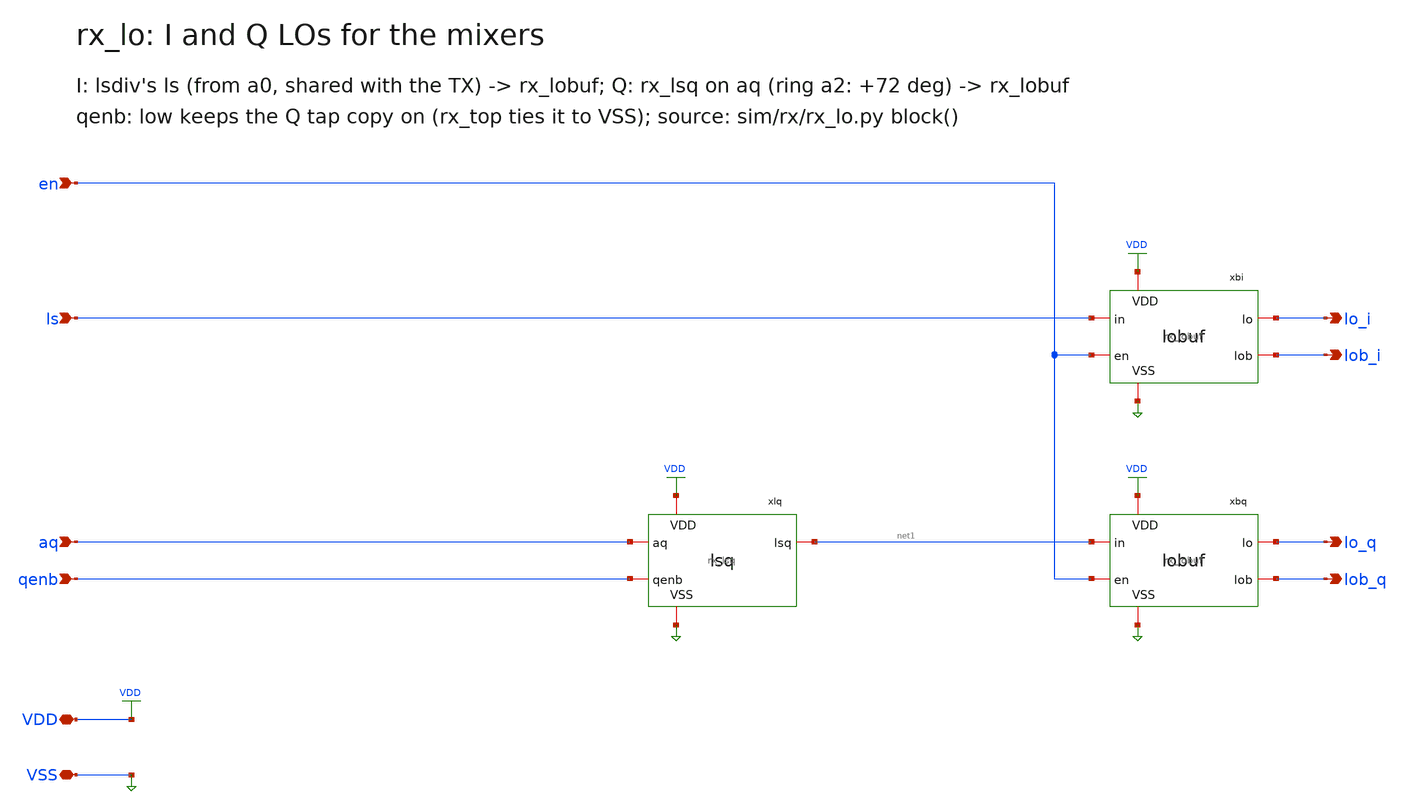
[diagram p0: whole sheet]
** sch_path: xschem/rx_lo.sch
**.subckt rx_lo VDD VSS ls aq en qenb lo_i lob_i lo_q lob_q
*.iopin VDD
*.iopin VSS
*.ipin ls
*.ipin aq
*.ipin en
*.ipin qenb
*.opin lo_i
*.opin lob_i
*.opin lo_q
*.opin lob_q
xlq VDD VSS aq qenb net1 rx_lsq
xbi VDD VSS ls en lo_i lob_i rx_lobuf
xbq VDD VSS net1 en lo_q lob_q rx_lobuf
**.ends

* expanding   symbol:  rx_lsq.sym # of pins=5
** sym_path: xschem/rx_lsq.sym
** sch_path: xschem/rx_lsq.sch
.subckt rx_lsq VDD VSS aq qenb lsq
*.iopin VDD
*.iopin VSS
*.ipin aq
*.ipin qenb
*.opin lsq
XHq net2 qenb VDD VDD pfet_03v3 L=0.28u W=10.0u nf=1 ad=5.0p as=5.0p pd=21.0u ps=21.0u nrd=0 nrs=0
+ sa=0 sb=0 sd=0 m=2
XCq VSS net2 VSS VSS nfet_03v3 L=10.0u W=24.57u nf=1 ad=12.285p as=12.285p pd=50.14u ps=50.14u nrd=0
+ nrs=0 sa=0 sb=0 sd=0 m=1
xls net2 VSS aq lsq ls_ac
xd1 net2 VSS lsq net3 tspc_t1
XTTp net1 lsq net2 net2 pfet_03v3 L=0.28u W=1.0499999999999998u nf=1 ad=0.5249999999999999p
+ as=0.5249999999999999p pd=3.0999999999999996u ps=3.0999999999999996u nrd=0 nrs=0 sa=0 sb=0 sd=0 m=1
XTTn net1 lsq VSS VSS nfet_03v3 L=0.28u W=0.41999999999999993u nf=1 ad=0.20999999999999996p
+ as=0.20999999999999996p pd=1.8399999999999999u ps=1.8399999999999999u nrd=0 nrs=0 sa=0 sb=0 sd=0 m=1
XDq lsq qenb VSS VSS nfet_03v3 L=0.28u W=0.41999999999999993u nf=1 ad=0.20999999999999996p
+ as=0.20999999999999996p pd=1.8399999999999999u ps=1.8399999999999999u nrd=0 nrs=0 sa=0 sb=0 sd=0 m=1
.ends


* expanding   symbol:  rx_lobuf.sym # of pins=6
** sym_path: xschem/rx_lobuf.sym
** sch_path: xschem/rx_lobuf.sch
.subckt rx_lobuf VDD VSS in en lo lob
*.iopin VDD
*.iopin VSS
*.ipin in
*.ipin en
*.opin lo
*.opin lob
XG0a net1 in VDD VDD pfet_03v3 L=0.28u W=0.6u nf=1 ad=0.3p as=0.3p pd=2.2u ps=2.2u nrd=0 nrs=0 sa=0
+ sb=0 sd=0 m=1
XG0b net1 en VDD VDD pfet_03v3 L=0.28u W=0.6u nf=1 ad=0.3p as=0.3p pd=2.2u ps=2.2u nrd=0 nrs=0 sa=0
+ sb=0 sd=0 m=1
XG0c net1 in net2 VSS nfet_03v3 L=0.28u W=0.5u nf=1 ad=0.25p as=0.25p pd=2.0u ps=2.0u nrd=0 nrs=0
+ sa=0 sb=0 sd=0 m=1
XG0d net2 en VSS VSS nfet_03v3 L=0.28u W=0.5u nf=1 ad=0.25p as=0.25p pd=2.0u ps=2.0u nrd=0 nrs=0
+ sa=0 sb=0 sd=0 m=1
XTp net3 net1 VDD VDD pfet_03v3 L=0.28u W=1.0499999999999998u nf=1 ad=0.5249999999999999p
+ as=0.5249999999999999p pd=3.0999999999999996u ps=3.0999999999999996u nrd=0 nrs=0 sa=0 sb=0 sd=0 m=1
XTn net3 net1 VSS VSS nfet_03v3 L=0.28u W=0.41999999999999993u nf=1 ad=0.20999999999999996p
+ as=0.20999999999999996p pd=1.8399999999999999u ps=1.8399999999999999u nrd=0 nrs=0 sa=0 sb=0 sd=0 m=1
XA1p net4 net3 VDD VDD pfet_03v3 L=0.28u W=1.25u nf=1 ad=0.625p as=0.625p pd=3.5u ps=3.5u nrd=0
+ nrs=0 sa=0 sb=0 sd=0 m=1
XA1n net4 net3 VSS VSS nfet_03v3 L=0.28u W=0.5u nf=1 ad=0.25p as=0.25p pd=2.0u ps=2.0u nrd=0 nrs=0
+ sa=0 sb=0 sd=0 m=1
XA2p net5 net4 VDD VDD pfet_03v3 L=0.28u W=2.5u nf=1 ad=1.25p as=1.25p pd=6.0u ps=6.0u nrd=0 nrs=0
+ sa=0 sb=0 sd=0 m=1
XA2n net5 net4 VSS VSS nfet_03v3 L=0.28u W=1.0u nf=1 ad=0.5p as=0.5p pd=3.0u ps=3.0u nrd=0 nrs=0
+ sa=0 sb=0 sd=0 m=1
XB1p net6 net3 VDD VDD pfet_03v3 L=0.28u W=3.7499999999999996u nf=1 ad=1.8749999999999998p
+ as=1.8749999999999998p pd=8.5u ps=8.5u nrd=0 nrs=0 sa=0 sb=0 sd=0 m=1
XB1n net6 net3 VSS VSS nfet_03v3 L=0.28u W=1.5u nf=1 ad=0.75p as=0.75p pd=4.0u ps=4.0u nrd=0 nrs=0
+ sa=0 sb=0 sd=0 m=1
XTGp net7 VSS net6 VDD pfet_03v3 L=0.28u W=2.5u nf=1 ad=1.25p as=1.25p pd=6.0u ps=6.0u nrd=0 nrs=0
+ sa=0 sb=0 sd=0 m=1
XTGn net7 VDD net6 VSS nfet_03v3 L=0.28u W=1.0u nf=1 ad=0.5p as=0.5p pd=3.0u ps=3.0u nrd=0 nrs=0
+ sa=0 sb=0 sd=0 m=1
XXBp net7 net5 VDD VDD pfet_03v3 L=0.28u W=1.0499999999999998u nf=1 ad=0.5249999999999999p
+ as=0.5249999999999999p pd=3.0999999999999996u ps=3.0999999999999996u nrd=0 nrs=0 sa=0 sb=0 sd=0 m=1
XXBn net7 net5 VSS VSS nfet_03v3 L=0.28u W=0.41999999999999993u nf=1 ad=0.20999999999999996p
+ as=0.20999999999999996p pd=1.8399999999999999u ps=1.8399999999999999u nrd=0 nrs=0 sa=0 sb=0 sd=0 m=1
XXAp net5 net7 VDD VDD pfet_03v3 L=0.28u W=1.0499999999999998u nf=1 ad=0.5249999999999999p
+ as=0.5249999999999999p pd=3.0999999999999996u ps=3.0999999999999996u nrd=0 nrs=0 sa=0 sb=0 sd=0 m=1
XXAn net5 net7 VSS VSS nfet_03v3 L=0.28u W=0.41999999999999993u nf=1 ad=0.20999999999999996p
+ as=0.20999999999999996p pd=1.8399999999999999u ps=1.8399999999999999u nrd=0 nrs=0 sa=0 sb=0 sd=0 m=1
XPGa net8 net5 VDD VDD pfet_03v3 L=0.28u W=1.25u nf=1 ad=0.625p as=0.625p pd=3.5u ps=3.5u nrd=0
+ nrs=0 sa=0 sb=0 sd=0 m=1
XPGb net8 en VDD VDD pfet_03v3 L=0.28u W=1.25u nf=1 ad=0.625p as=0.625p pd=3.5u ps=3.5u nrd=0 nrs=0
+ sa=0 sb=0 sd=0 m=1
XPGc net8 net5 net9 VSS nfet_03v3 L=0.28u W=1.0u nf=1 ad=0.5p as=0.5p pd=3.0u ps=3.0u nrd=0 nrs=0
+ sa=0 sb=0 sd=0 m=1
XPGd net9 en VSS VSS nfet_03v3 L=0.28u W=1.0u nf=1 ad=0.5p as=0.5p pd=3.0u ps=3.0u nrd=0 nrs=0 sa=0
+ sb=0 sd=0 m=1
XP1p net10 net8 VDD VDD pfet_03v3 L=0.28u W=2.0u nf=1 ad=1.0p as=1.0p pd=5.0u ps=5.0u nrd=0 nrs=0
+ sa=0 sb=0 sd=0 m=1
XP1n net10 net8 VSS VSS nfet_03v3 L=0.28u W=0.7999999999999999u nf=1 ad=0.39999999999999997p
+ as=0.39999999999999997p pd=2.5999999999999996u ps=2.5999999999999996u nrd=0 nrs=0 sa=0 sb=0 sd=0 m=1
XP2p net11 net10 VDD VDD pfet_03v3 L=0.28u W=5.0u nf=1 ad=2.5p as=2.5p pd=11.0u ps=11.0u nrd=0 nrs=0
+ sa=0 sb=0 sd=0 m=1
XP2n net11 net10 VSS VSS nfet_03v3 L=0.28u W=2.0u nf=1 ad=1.0p as=1.0p pd=5.0u ps=5.0u nrd=0 nrs=0
+ sa=0 sb=0 sd=0 m=1
XP3p lo net11 VDD VDD pfet_03v3 L=0.28u W=12.499999999999998u nf=1 ad=6.249999999999999p
+ as=6.249999999999999p pd=25.999999999999996u ps=25.999999999999996u nrd=0 nrs=0 sa=0 sb=0 sd=0 m=1
XP3n lo net11 VSS VSS nfet_03v3 L=0.28u W=5.0u nf=1 ad=2.5p as=2.5p pd=11.0u ps=11.0u nrd=0 nrs=0
+ sa=0 sb=0 sd=0 m=1
XNGa net12 net7 VDD VDD pfet_03v3 L=0.28u W=1.25u nf=1 ad=0.625p as=0.625p pd=3.5u ps=3.5u nrd=0
+ nrs=0 sa=0 sb=0 sd=0 m=1
XNGb net12 en VDD VDD pfet_03v3 L=0.28u W=1.25u nf=1 ad=0.625p as=0.625p pd=3.5u ps=3.5u nrd=0 nrs=0
+ sa=0 sb=0 sd=0 m=1
XNGc net12 net7 net13 VSS nfet_03v3 L=0.28u W=1.0u nf=1 ad=0.5p as=0.5p pd=3.0u ps=3.0u nrd=0 nrs=0
+ sa=0 sb=0 sd=0 m=1
XNGd net13 en VSS VSS nfet_03v3 L=0.28u W=1.0u nf=1 ad=0.5p as=0.5p pd=3.0u ps=3.0u nrd=0 nrs=0 sa=0
+ sb=0 sd=0 m=1
XN1p net14 net12 VDD VDD pfet_03v3 L=0.28u W=2.0u nf=1 ad=1.0p as=1.0p pd=5.0u ps=5.0u nrd=0 nrs=0
+ sa=0 sb=0 sd=0 m=1
XN1n net14 net12 VSS VSS nfet_03v3 L=0.28u W=0.7999999999999999u nf=1 ad=0.39999999999999997p
+ as=0.39999999999999997p pd=2.5999999999999996u ps=2.5999999999999996u nrd=0 nrs=0 sa=0 sb=0 sd=0 m=1
XN2p net15 net14 VDD VDD pfet_03v3 L=0.28u W=5.0u nf=1 ad=2.5p as=2.5p pd=11.0u ps=11.0u nrd=0 nrs=0
+ sa=0 sb=0 sd=0 m=1
XN2n net15 net14 VSS VSS nfet_03v3 L=0.28u W=2.0u nf=1 ad=1.0p as=1.0p pd=5.0u ps=5.0u nrd=0 nrs=0
+ sa=0 sb=0 sd=0 m=1
XN3p lob net15 VDD VDD pfet_03v3 L=0.28u W=12.499999999999998u nf=1 ad=6.249999999999999p
+ as=6.249999999999999p pd=25.999999999999996u ps=25.999999999999996u nrd=0 nrs=0 sa=0 sb=0 sd=0 m=1
XN3n lob net15 VSS VSS nfet_03v3 L=0.28u W=5.0u nf=1 ad=2.5p as=2.5p pd=11.0u ps=11.0u nrd=0 nrs=0
+ sa=0 sb=0 sd=0 m=1
.ends


* expanding   symbol:  ls_ac.sym # of pins=4
** sym_path: xschem/ls_ac.sym
** sch_path: xschem/ls_ac.sch
.subckt ls_ac VDD VSS a0 ls
*.iopin VDD
*.iopin VSS
*.ipin a0
*.opin ls
XL1p net2 net1 VDD VDD pfet_03v3 L=0.28u W=0.5u nf=1 ad=0.25p as=0.25p pd=2.0u ps=2.0u nrd=0 nrs=0
+ sa=0 sb=0 sd=0 m=1
XL1n net2 net1 VSS VSS nfet_03v3 L=0.28u W=0.21999999999999997u nf=1 ad=0.10999999999999999p
+ as=0.10999999999999999p pd=1.44u ps=1.44u nrd=0 nrs=0 sa=0 sb=0 sd=0 m=1
XL2p net3 net2 VDD VDD pfet_03v3 L=0.28u W=1.5u nf=1 ad=0.75p as=0.75p pd=4.0u ps=4.0u nrd=0 nrs=0
+ sa=0 sb=0 sd=0 m=1
XL2n net3 net2 VSS VSS nfet_03v3 L=0.28u W=0.6u nf=1 ad=0.3p as=0.3p pd=2.2u ps=2.2u nrd=0 nrs=0
+ sa=0 sb=0 sd=0 m=1
XL3p ls net3 VDD VDD pfet_03v3 L=0.28u W=3.0u nf=1 ad=1.5p as=1.5p pd=7.0u ps=7.0u nrd=0 nrs=0 sa=0
+ sb=0 sd=0 m=1
XL3n ls net3 VSS VSS nfet_03v3 L=0.28u W=1.2u nf=1 ad=0.6p as=0.6p pd=3.4u ps=3.4u nrd=0 nrs=0 sa=0
+ sb=0 sd=0 m=1
Cc a0 net1 2e-15 m=1
XLRB net1 VSS net4 VDD pfet_03v3 L=2.0u W=0.21999999999999997u nf=1 ad=0.10999999999999999p
+ as=0.10999999999999999p pd=1.44u ps=1.44u nrd=0 nrs=0 sa=0 sb=0 sd=0 m=1
XR1 ls net4 VSS ppolyf_u_1k r_width=1.0e-6 r_length=159.125e-6 m=1
XC1 VSS net4 VSS VSS nfet_03v3 L=16.0u W=16.0u nf=1 ad=8.0p as=8.0p pd=33.0u ps=33.0u nrd=0 nrs=0
+ sa=0 sb=0 sd=0 m=1
.ends


* expanding   symbol:  tspc_t1.sym # of pins=4
** sym_path: xschem/tspc_t1.sym
** sch_path: xschem/tspc_t1.sch
.subckt tspc_t1 VDD VSS clk q
*.iopin VDD
*.iopin VSS
*.ipin clk
*.opin q
Xp1 net1 net6 VDD VDD pfet_03v3 L=0.28u W=2.0u nf=1 ad=1.0p as=1.0p pd=5.0u ps=5.0u nrd=0 nrs=0 sa=0
+ sb=0 sd=0 m=1
Xp2 net4 clk net1 VDD pfet_03v3 L=0.28u W=2.0u nf=1 ad=1.0p as=1.0p pd=5.0u ps=5.0u nrd=0 nrs=0 sa=0
+ sb=0 sd=0 m=1
Xn1 net4 net6 VSS VSS nfet_03v3 L=0.28u W=1.0u nf=1 ad=0.5p as=0.5p pd=3.0u ps=3.0u nrd=0 nrs=0 sa=0
+ sb=0 sd=0 m=1
Xp3 net5 clk VDD VDD pfet_03v3 L=0.28u W=2.0u nf=1 ad=1.0p as=1.0p pd=5.0u ps=5.0u nrd=0 nrs=0 sa=0
+ sb=0 sd=0 m=1
Xn2 net5 net4 net2 VSS nfet_03v3 L=0.28u W=1.0u nf=1 ad=0.5p as=0.5p pd=3.0u ps=3.0u nrd=0 nrs=0
+ sa=0 sb=0 sd=0 m=1
Xn3 net2 clk VSS VSS nfet_03v3 L=0.28u W=1.0u nf=1 ad=0.5p as=0.5p pd=3.0u ps=3.0u nrd=0 nrs=0 sa=0
+ sb=0 sd=0 m=1
Xp4 net6 net5 VDD VDD pfet_03v3 L=0.28u W=2.0u nf=1 ad=1.0p as=1.0p pd=5.0u ps=5.0u nrd=0 nrs=0 sa=0
+ sb=0 sd=0 m=1
Xn4 net6 clk net3 VSS nfet_03v3 L=0.28u W=1.0u nf=1 ad=0.5p as=0.5p pd=3.0u ps=3.0u nrd=0 nrs=0 sa=0
+ sb=0 sd=0 m=1
Xn5 net3 net5 VSS VSS nfet_03v3 L=0.28u W=1.0u nf=1 ad=0.5p as=0.5p pd=3.0u ps=3.0u nrd=0 nrs=0 sa=0
+ sb=0 sd=0 m=1
Xqp q net6 VDD VDD pfet_03v3 L=0.28u W=1.5u nf=1 ad=0.75p as=0.75p pd=4.0u ps=4.0u nrd=0 nrs=0 sa=0
+ sb=0 sd=0 m=1
Xqn q net6 VSS VSS nfet_03v3 L=0.28u W=0.6u nf=1 ad=0.3p as=0.3p pd=2.2u ps=2.2u nrd=0 nrs=0 sa=0
+ sb=0 sd=0 m=1
.ends

.end
